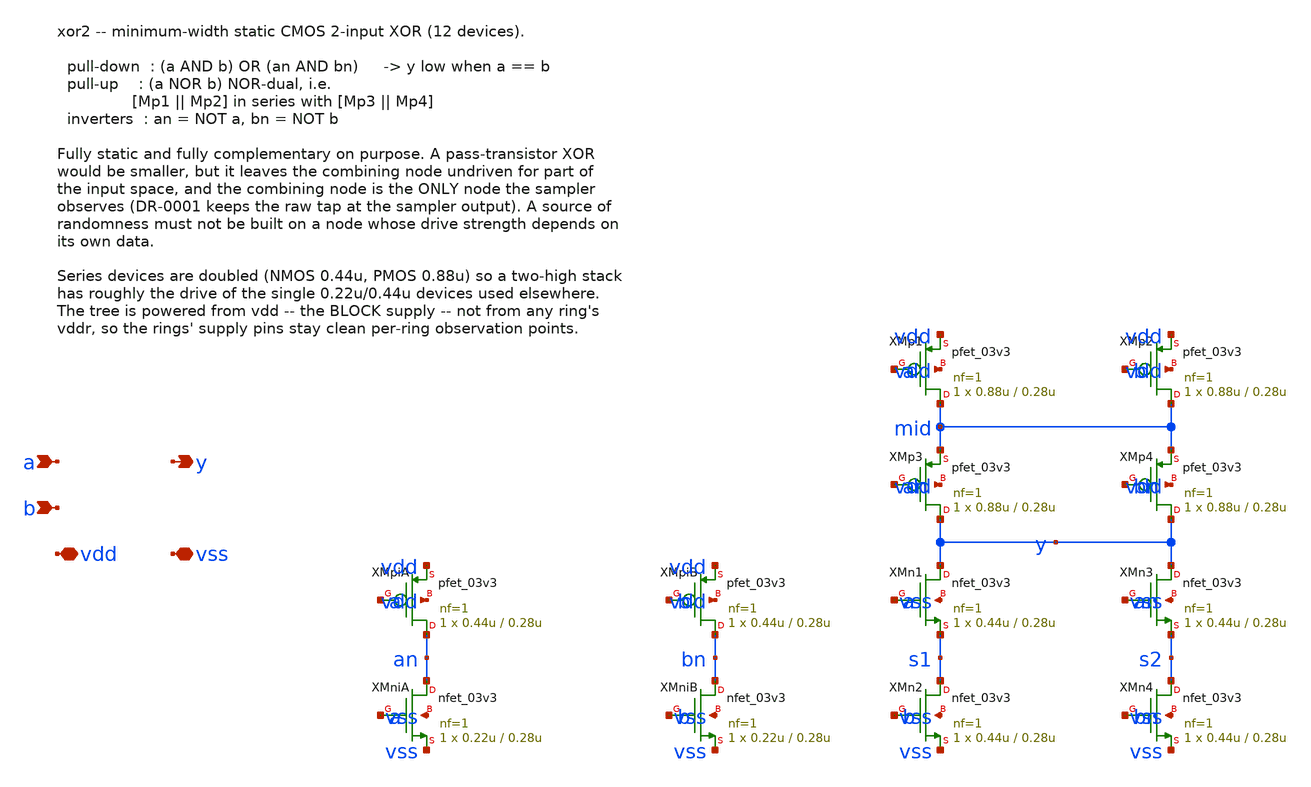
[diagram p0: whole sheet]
** sch_path: design/xschem/xor2.sch
**.subckt xor2 a b y vdd vss
*.ipin a
*.ipin b
*.opin y
*.iopin vdd
*.iopin vss
XMpiA an a vdd vdd pfet_03v3 L=0.28u W=0.44u nf=1 ad='int((nf+1)/2) * W/nf * 0.18u' as='int((nf+2)/2) * W/nf * 0.18u'
+ pd='2*int((nf+1)/2) * (W/nf + 0.18u)' ps='2*int((nf+2)/2) * (W/nf + 0.18u)' nrd='0.18u / W' nrs='0.18u / W'
+ sa=0 sb=0 sd=0 m=1
XMniA an a vss vss nfet_03v3 L=0.28u W=0.22u nf=1 ad='int((nf+1)/2) * W/nf * 0.18u' as='int((nf+2)/2) * W/nf * 0.18u'
+ pd='2*int((nf+1)/2) * (W/nf + 0.18u)' ps='2*int((nf+2)/2) * (W/nf + 0.18u)' nrd='0.18u / W' nrs='0.18u / W'
+ sa=0 sb=0 sd=0 m=1
XMpiB bn b vdd vdd pfet_03v3 L=0.28u W=0.44u nf=1 ad='int((nf+1)/2) * W/nf * 0.18u' as='int((nf+2)/2) * W/nf * 0.18u'
+ pd='2*int((nf+1)/2) * (W/nf + 0.18u)' ps='2*int((nf+2)/2) * (W/nf + 0.18u)' nrd='0.18u / W' nrs='0.18u / W'
+ sa=0 sb=0 sd=0 m=1
XMniB bn b vss vss nfet_03v3 L=0.28u W=0.22u nf=1 ad='int((nf+1)/2) * W/nf * 0.18u' as='int((nf+2)/2) * W/nf * 0.18u'
+ pd='2*int((nf+1)/2) * (W/nf + 0.18u)' ps='2*int((nf+2)/2) * (W/nf + 0.18u)' nrd='0.18u / W' nrs='0.18u / W'
+ sa=0 sb=0 sd=0 m=1
XMp1 mid a vdd vdd pfet_03v3 L=0.28u W=0.88u nf=1 ad='int((nf+1)/2) * W/nf * 0.18u' as='int((nf+2)/2) * W/nf * 0.18u'
+ pd='2*int((nf+1)/2) * (W/nf + 0.18u)' ps='2*int((nf+2)/2) * (W/nf + 0.18u)' nrd='0.18u / W' nrs='0.18u / W'
+ sa=0 sb=0 sd=0 m=1
XMp2 mid b vdd vdd pfet_03v3 L=0.28u W=0.88u nf=1 ad='int((nf+1)/2) * W/nf * 0.18u' as='int((nf+2)/2) * W/nf * 0.18u'
+ pd='2*int((nf+1)/2) * (W/nf + 0.18u)' ps='2*int((nf+2)/2) * (W/nf + 0.18u)' nrd='0.18u / W' nrs='0.18u / W'
+ sa=0 sb=0 sd=0 m=1
XMp3 y an mid vdd pfet_03v3 L=0.28u W=0.88u nf=1 ad='int((nf+1)/2) * W/nf * 0.18u' as='int((nf+2)/2) * W/nf * 0.18u'
+ pd='2*int((nf+1)/2) * (W/nf + 0.18u)' ps='2*int((nf+2)/2) * (W/nf + 0.18u)' nrd='0.18u / W' nrs='0.18u / W'
+ sa=0 sb=0 sd=0 m=1
XMp4 y bn mid vdd pfet_03v3 L=0.28u W=0.88u nf=1 ad='int((nf+1)/2) * W/nf * 0.18u' as='int((nf+2)/2) * W/nf * 0.18u'
+ pd='2*int((nf+1)/2) * (W/nf + 0.18u)' ps='2*int((nf+2)/2) * (W/nf + 0.18u)' nrd='0.18u / W' nrs='0.18u / W'
+ sa=0 sb=0 sd=0 m=1
XMn1 y a s1 vss nfet_03v3 L=0.28u W=0.44u nf=1 ad='int((nf+1)/2) * W/nf * 0.18u' as='int((nf+2)/2) * W/nf * 0.18u'
+ pd='2*int((nf+1)/2) * (W/nf + 0.18u)' ps='2*int((nf+2)/2) * (W/nf + 0.18u)' nrd='0.18u / W' nrs='0.18u / W'
+ sa=0 sb=0 sd=0 m=1
XMn2 s1 b vss vss nfet_03v3 L=0.28u W=0.44u nf=1 ad='int((nf+1)/2) * W/nf * 0.18u' as='int((nf+2)/2) * W/nf * 0.18u'
+ pd='2*int((nf+1)/2) * (W/nf + 0.18u)' ps='2*int((nf+2)/2) * (W/nf + 0.18u)' nrd='0.18u / W' nrs='0.18u / W'
+ sa=0 sb=0 sd=0 m=1
XMn3 y an s2 vss nfet_03v3 L=0.28u W=0.44u nf=1 ad='int((nf+1)/2) * W/nf * 0.18u' as='int((nf+2)/2) * W/nf * 0.18u'
+ pd='2*int((nf+1)/2) * (W/nf + 0.18u)' ps='2*int((nf+2)/2) * (W/nf + 0.18u)' nrd='0.18u / W' nrs='0.18u / W'
+ sa=0 sb=0 sd=0 m=1
XMn4 s2 bn vss vss nfet_03v3 L=0.28u W=0.44u nf=1 ad='int((nf+1)/2) * W/nf * 0.18u' as='int((nf+2)/2) * W/nf * 0.18u'
+ pd='2*int((nf+1)/2) * (W/nf + 0.18u)' ps='2*int((nf+2)/2) * (W/nf + 0.18u)' nrd='0.18u / W' nrs='0.18u / W'
+ sa=0 sb=0 sd=0 m=1
**.ends
.end
